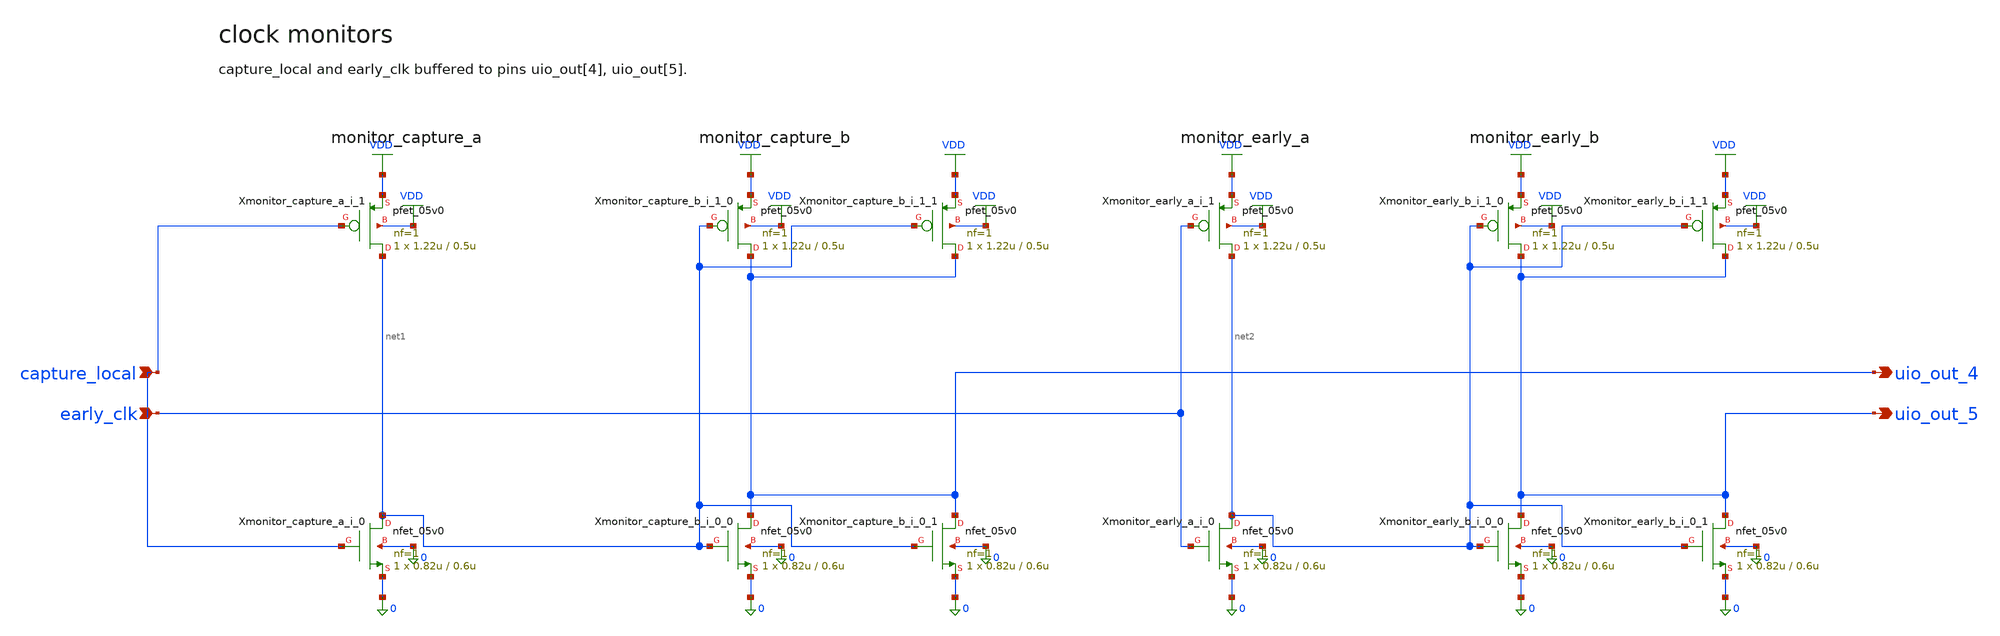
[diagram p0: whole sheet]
** sch_path: xschem/flat/monitors.sch
**.subckt monitors capture_local early_clk uio_out_4 uio_out_5
*.ipin capture_local
*.ipin early_clk
*.opin uio_out_4
*.opin uio_out_5
Xmonitor_capture_a_i_0 net1 capture_local 0 0 nfet_05v0 L=0.6u W=0.82u nf=1 ad=4.1e-13 as=4.1e-13
+ pd=2.64e-06 ps=2.64e-06 nrd=0 nrs=0 sa=0 sb=0 sd=0 m=1
Xmonitor_capture_a_i_1 net1 capture_local VDD VDD pfet_05v0 L=0.5u W=1.22u nf=1 ad=6.1e-13
+ as=6.1e-13 pd=3.44e-06 ps=3.44e-06 nrd=0 nrs=0 sa=0 sb=0 sd=0 m=1
Xmonitor_capture_b_i_0_0 uio_out_4 net1 0 0 nfet_05v0 L=0.6u W=0.82u nf=1 ad=4.1e-13 as=4.1e-13
+ pd=2.64e-06 ps=2.64e-06 nrd=0 nrs=0 sa=0 sb=0 sd=0 m=1
Xmonitor_capture_b_i_0_1 uio_out_4 net1 0 0 nfet_05v0 L=0.6u W=0.82u nf=1 ad=4.1e-13 as=4.1e-13
+ pd=2.64e-06 ps=2.64e-06 nrd=0 nrs=0 sa=0 sb=0 sd=0 m=1
Xmonitor_capture_b_i_1_0 uio_out_4 net1 VDD VDD pfet_05v0 L=0.5u W=1.22u nf=1 ad=6.1e-13 as=6.1e-13
+ pd=3.44e-06 ps=3.44e-06 nrd=0 nrs=0 sa=0 sb=0 sd=0 m=1
Xmonitor_capture_b_i_1_1 uio_out_4 net1 VDD VDD pfet_05v0 L=0.5u W=1.22u nf=1 ad=6.1e-13 as=6.1e-13
+ pd=3.44e-06 ps=3.44e-06 nrd=0 nrs=0 sa=0 sb=0 sd=0 m=1
Xmonitor_early_a_i_0 net2 early_clk 0 0 nfet_05v0 L=0.6u W=0.82u nf=1 ad=4.1e-13 as=4.1e-13
+ pd=2.64e-06 ps=2.64e-06 nrd=0 nrs=0 sa=0 sb=0 sd=0 m=1
Xmonitor_early_a_i_1 net2 early_clk VDD VDD pfet_05v0 L=0.5u W=1.22u nf=1 ad=6.1e-13 as=6.1e-13
+ pd=3.44e-06 ps=3.44e-06 nrd=0 nrs=0 sa=0 sb=0 sd=0 m=1
Xmonitor_early_b_i_0_0 uio_out_5 net2 0 0 nfet_05v0 L=0.6u W=0.82u nf=1 ad=4.1e-13 as=4.1e-13
+ pd=2.64e-06 ps=2.64e-06 nrd=0 nrs=0 sa=0 sb=0 sd=0 m=1
Xmonitor_early_b_i_0_1 uio_out_5 net2 0 0 nfet_05v0 L=0.6u W=0.82u nf=1 ad=4.1e-13 as=4.1e-13
+ pd=2.64e-06 ps=2.64e-06 nrd=0 nrs=0 sa=0 sb=0 sd=0 m=1
Xmonitor_early_b_i_1_0 uio_out_5 net2 VDD VDD pfet_05v0 L=0.5u W=1.22u nf=1 ad=6.1e-13 as=6.1e-13
+ pd=3.44e-06 ps=3.44e-06 nrd=0 nrs=0 sa=0 sb=0 sd=0 m=1
Xmonitor_early_b_i_1_1 uio_out_5 net2 VDD VDD pfet_05v0 L=0.5u W=1.22u nf=1 ad=6.1e-13 as=6.1e-13
+ pd=3.44e-06 ps=3.44e-06 nrd=0 nrs=0 sa=0 sb=0 sd=0 m=1
**.ends
.GLOBAL VDD
.end
